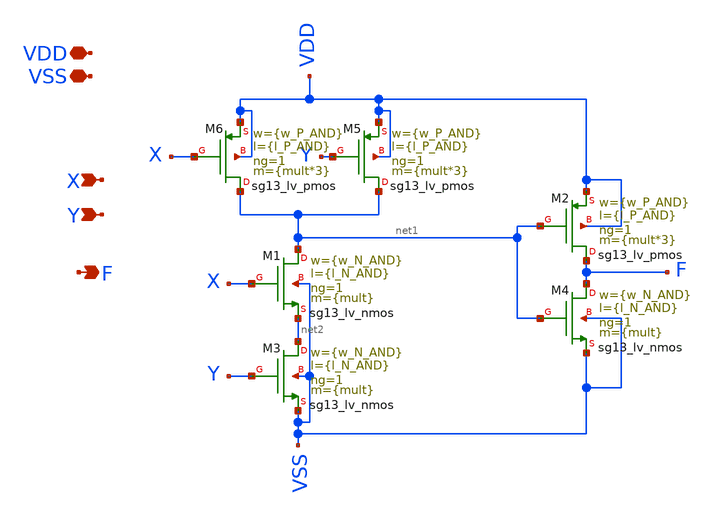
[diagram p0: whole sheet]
** sch_path: xschem/DigitalGates/AND.sch
**.subckt AND VDD X F VSS Y
*.iopin VDD
*.ipin X
*.opin F
*.iopin VSS
*.ipin Y
XM1 net1 X net2 VSS sg13_lv_nmos w={w_N_AND} l={l_N_AND} ng=1 m={mult} mm_ok=1
XM2 F net1 VDD VDD sg13_lv_pmos w={w_P_AND} l={l_P_AND} ng=1 m={mult*3} mm_ok=1
XM3 net2 Y VSS VSS sg13_lv_nmos w={w_N_AND} l={l_N_AND} ng=1 m={mult} mm_ok=1
XM4 F net1 VSS VSS sg13_lv_nmos w={w_N_AND} l={l_N_AND} ng=1 m={mult} mm_ok=1
XM5 net1 Y VDD VDD sg13_lv_pmos w={w_P_AND} l={l_P_AND} ng=1 m={mult*3} mm_ok=1
XM6 net1 X VDD VDD sg13_lv_pmos w={w_P_AND} l={l_P_AND} ng=1 m={mult*3} mm_ok=1
**** begin user architecture code



**** end user architecture code
**.ends
.end
